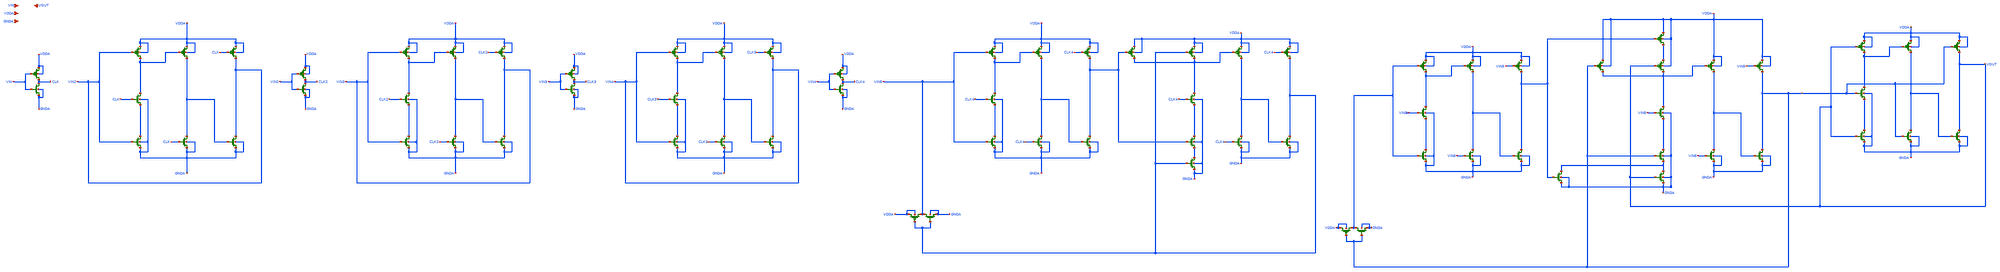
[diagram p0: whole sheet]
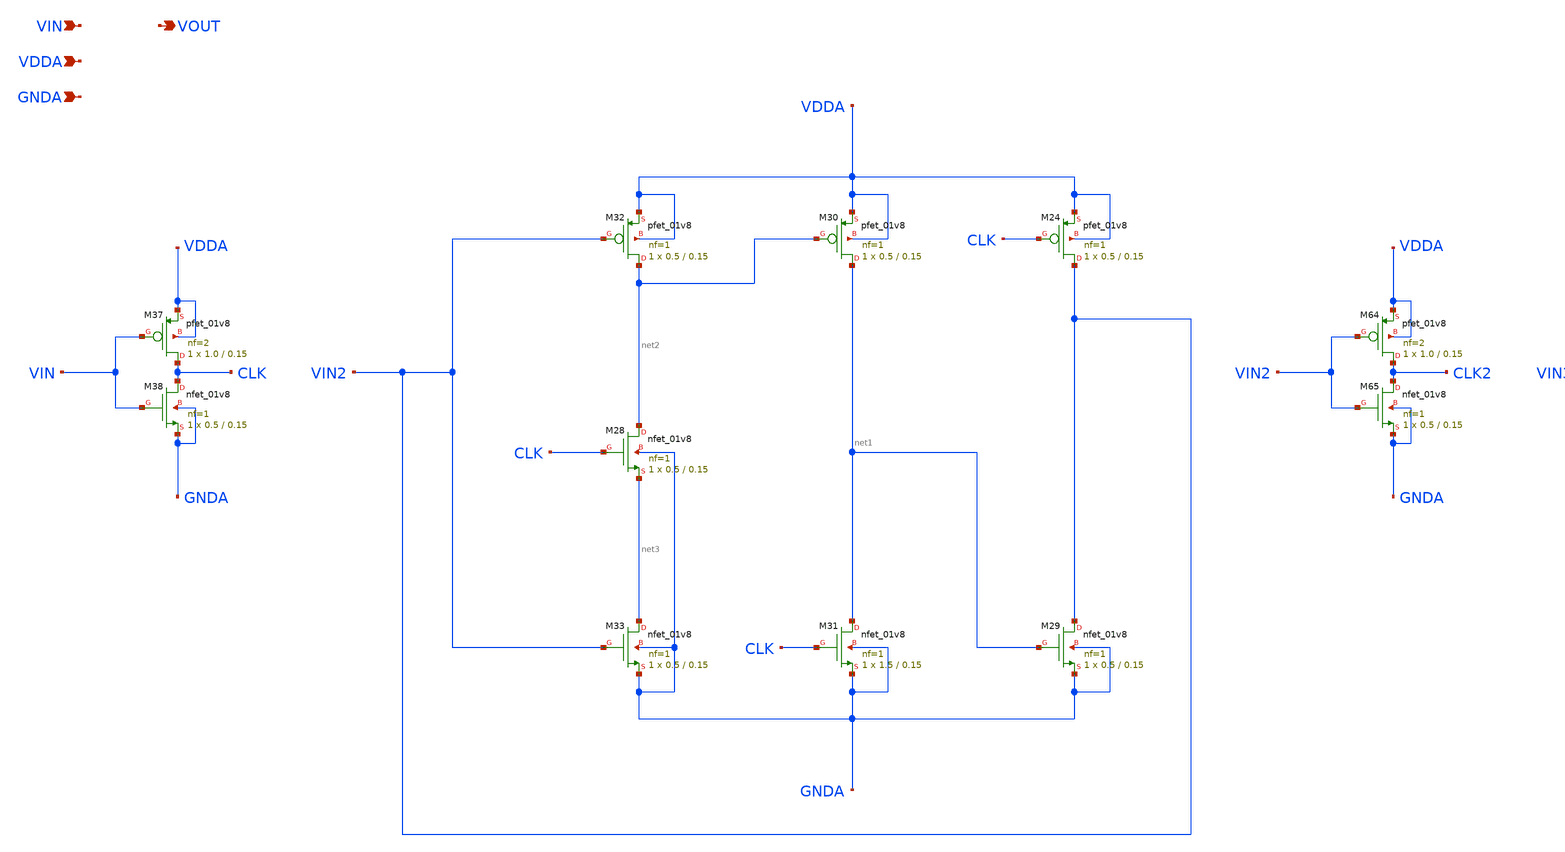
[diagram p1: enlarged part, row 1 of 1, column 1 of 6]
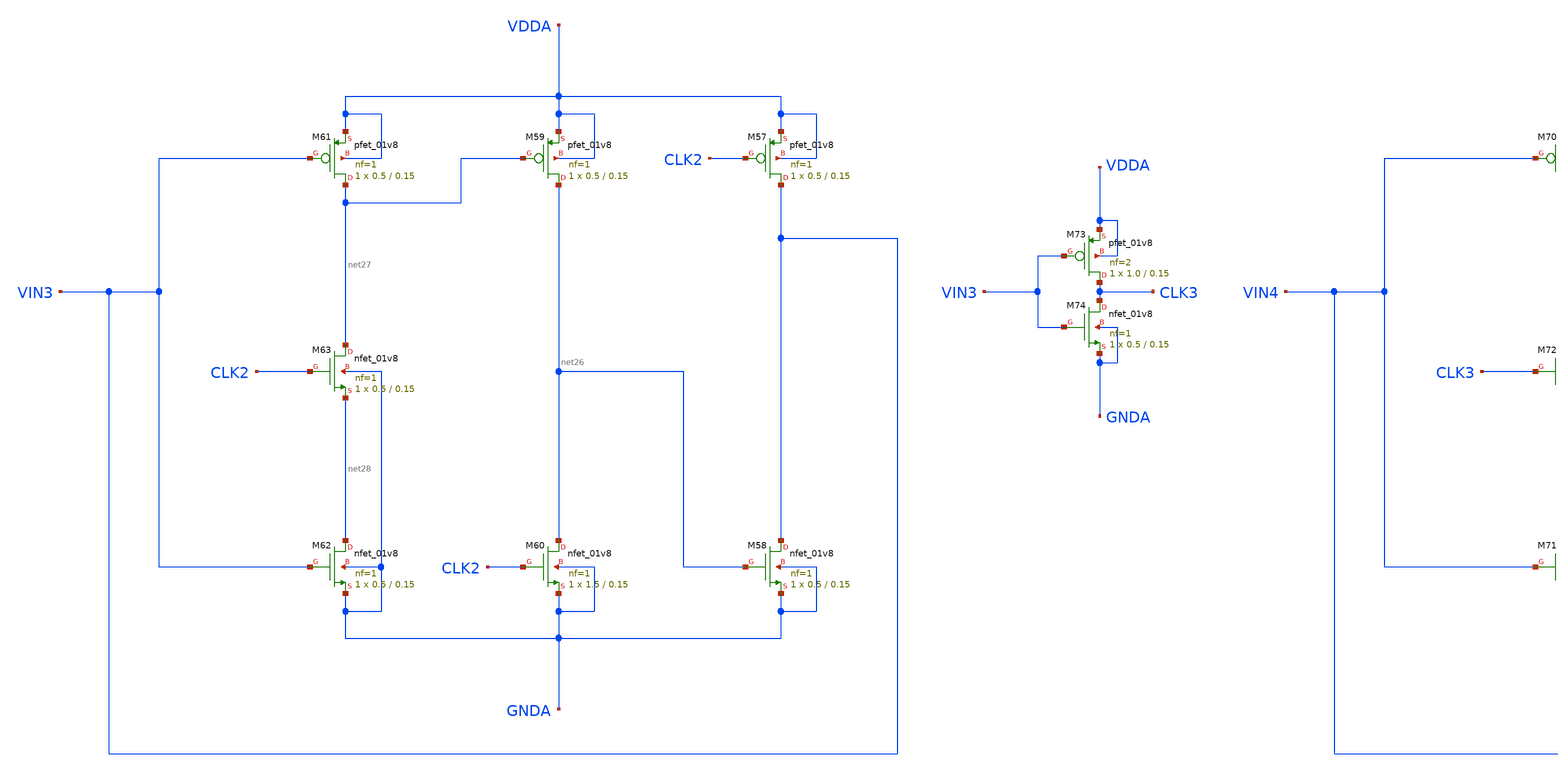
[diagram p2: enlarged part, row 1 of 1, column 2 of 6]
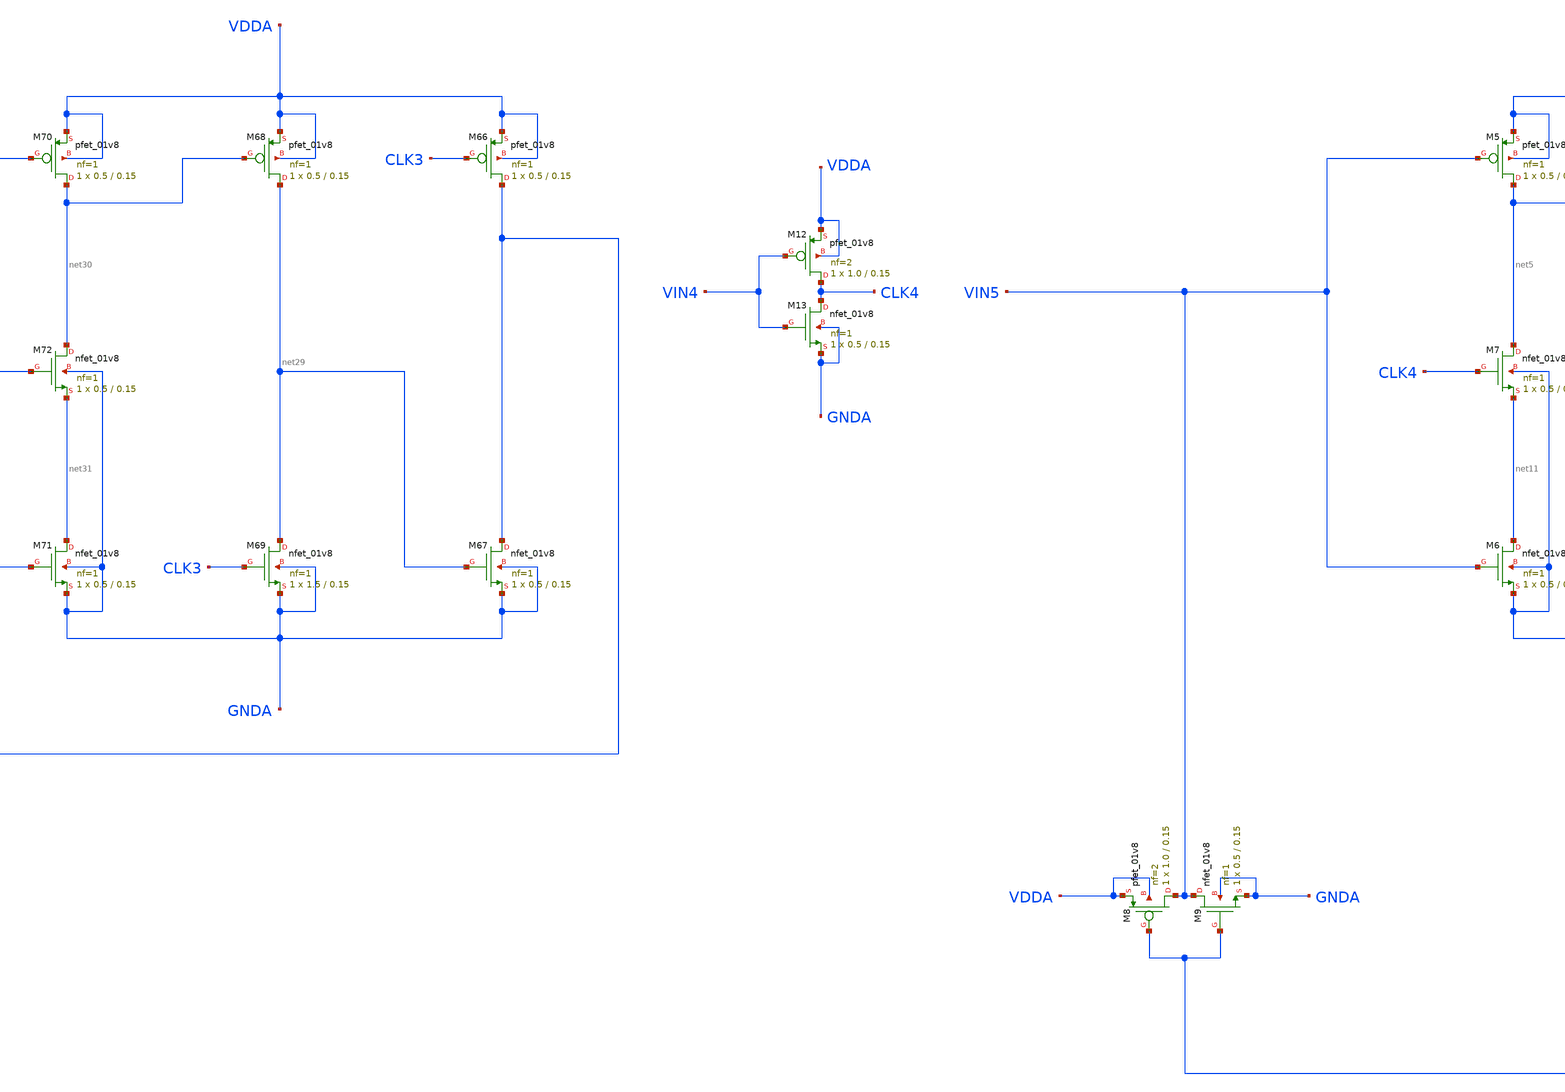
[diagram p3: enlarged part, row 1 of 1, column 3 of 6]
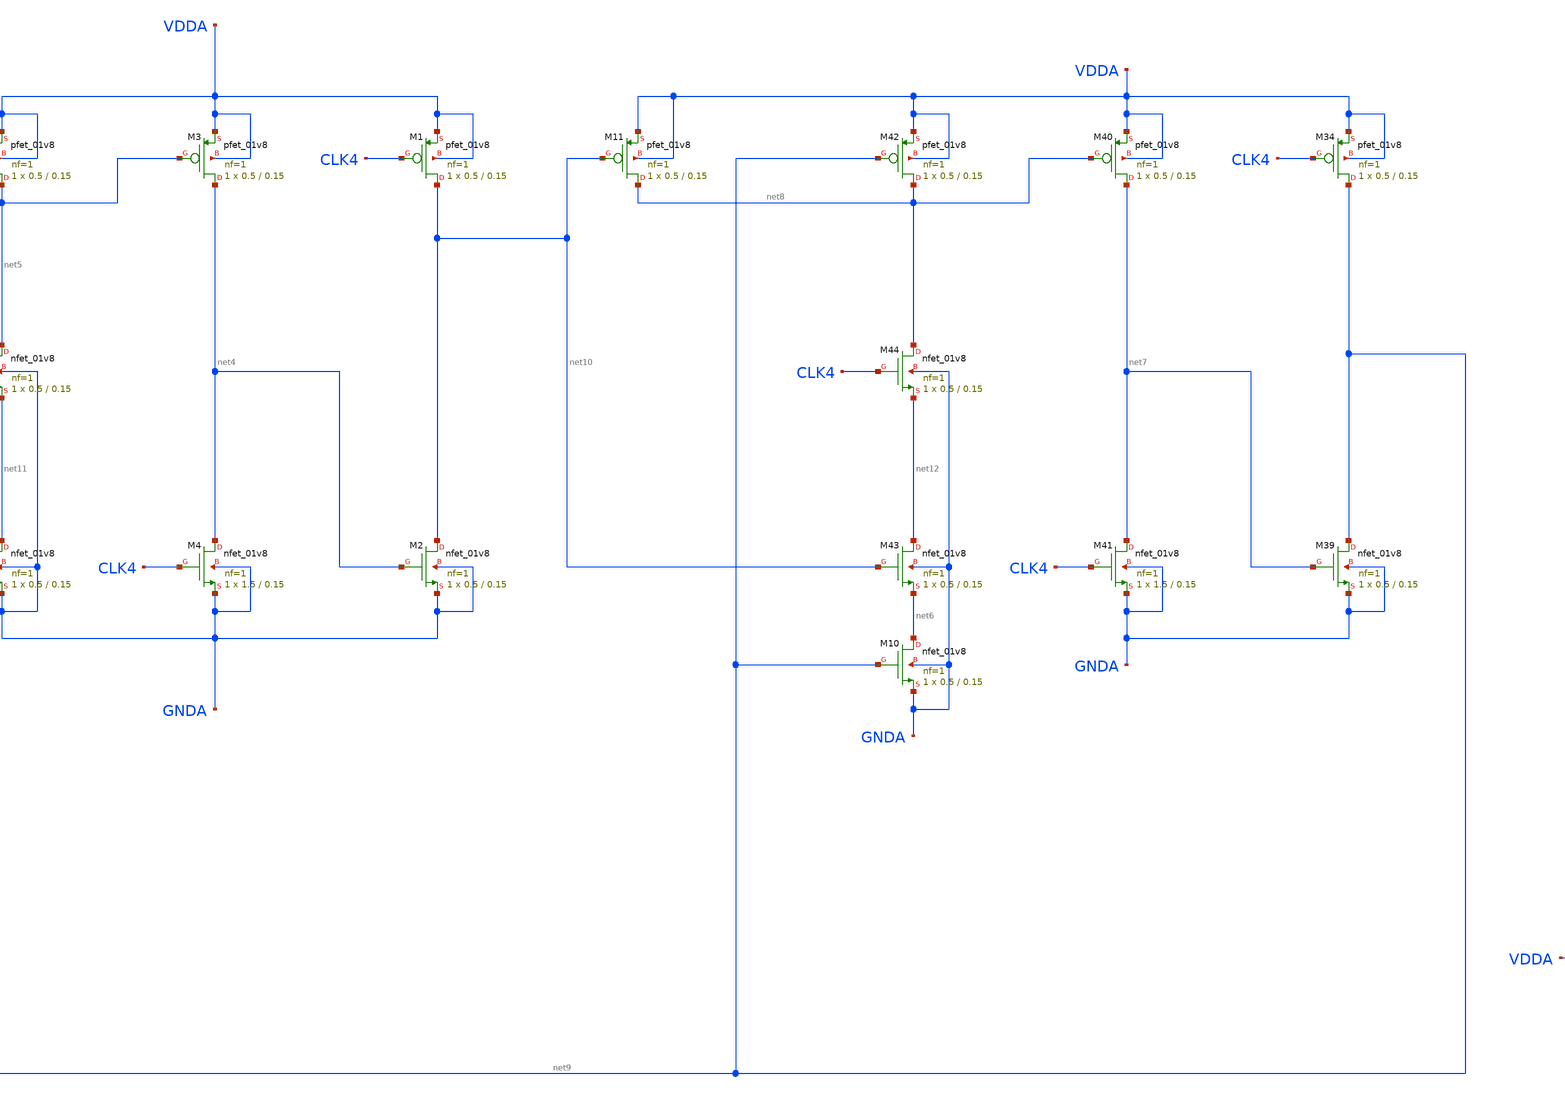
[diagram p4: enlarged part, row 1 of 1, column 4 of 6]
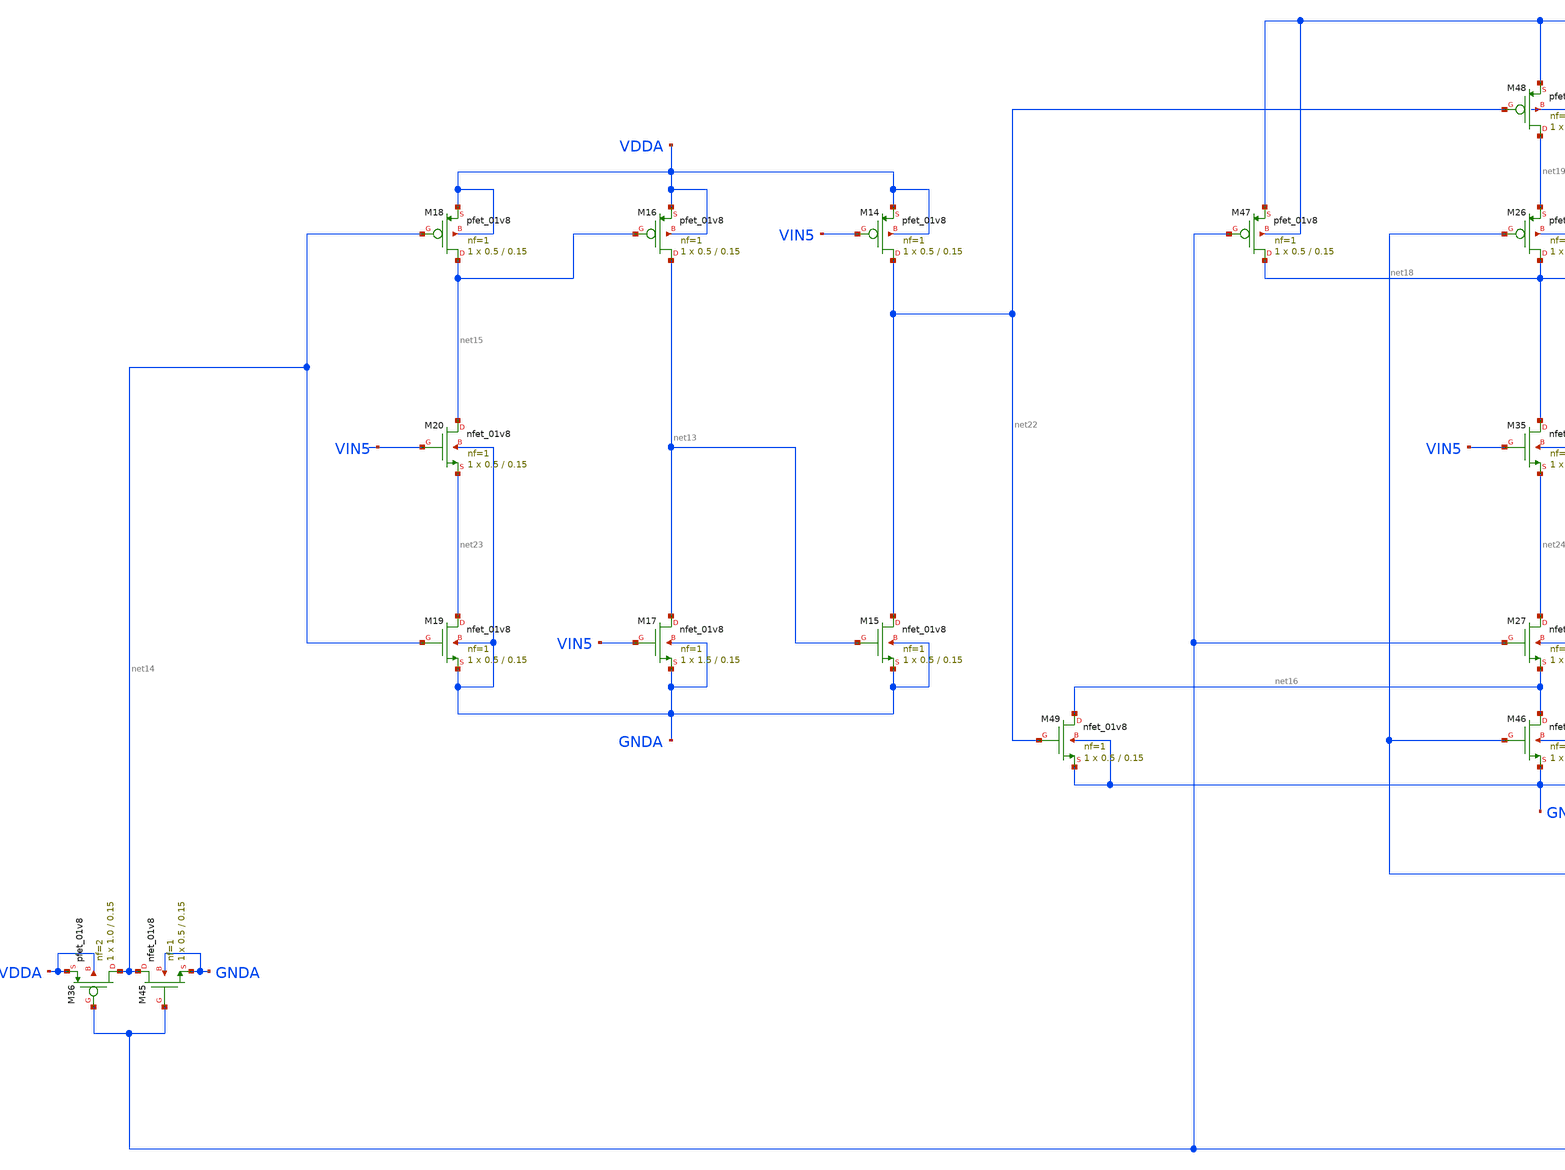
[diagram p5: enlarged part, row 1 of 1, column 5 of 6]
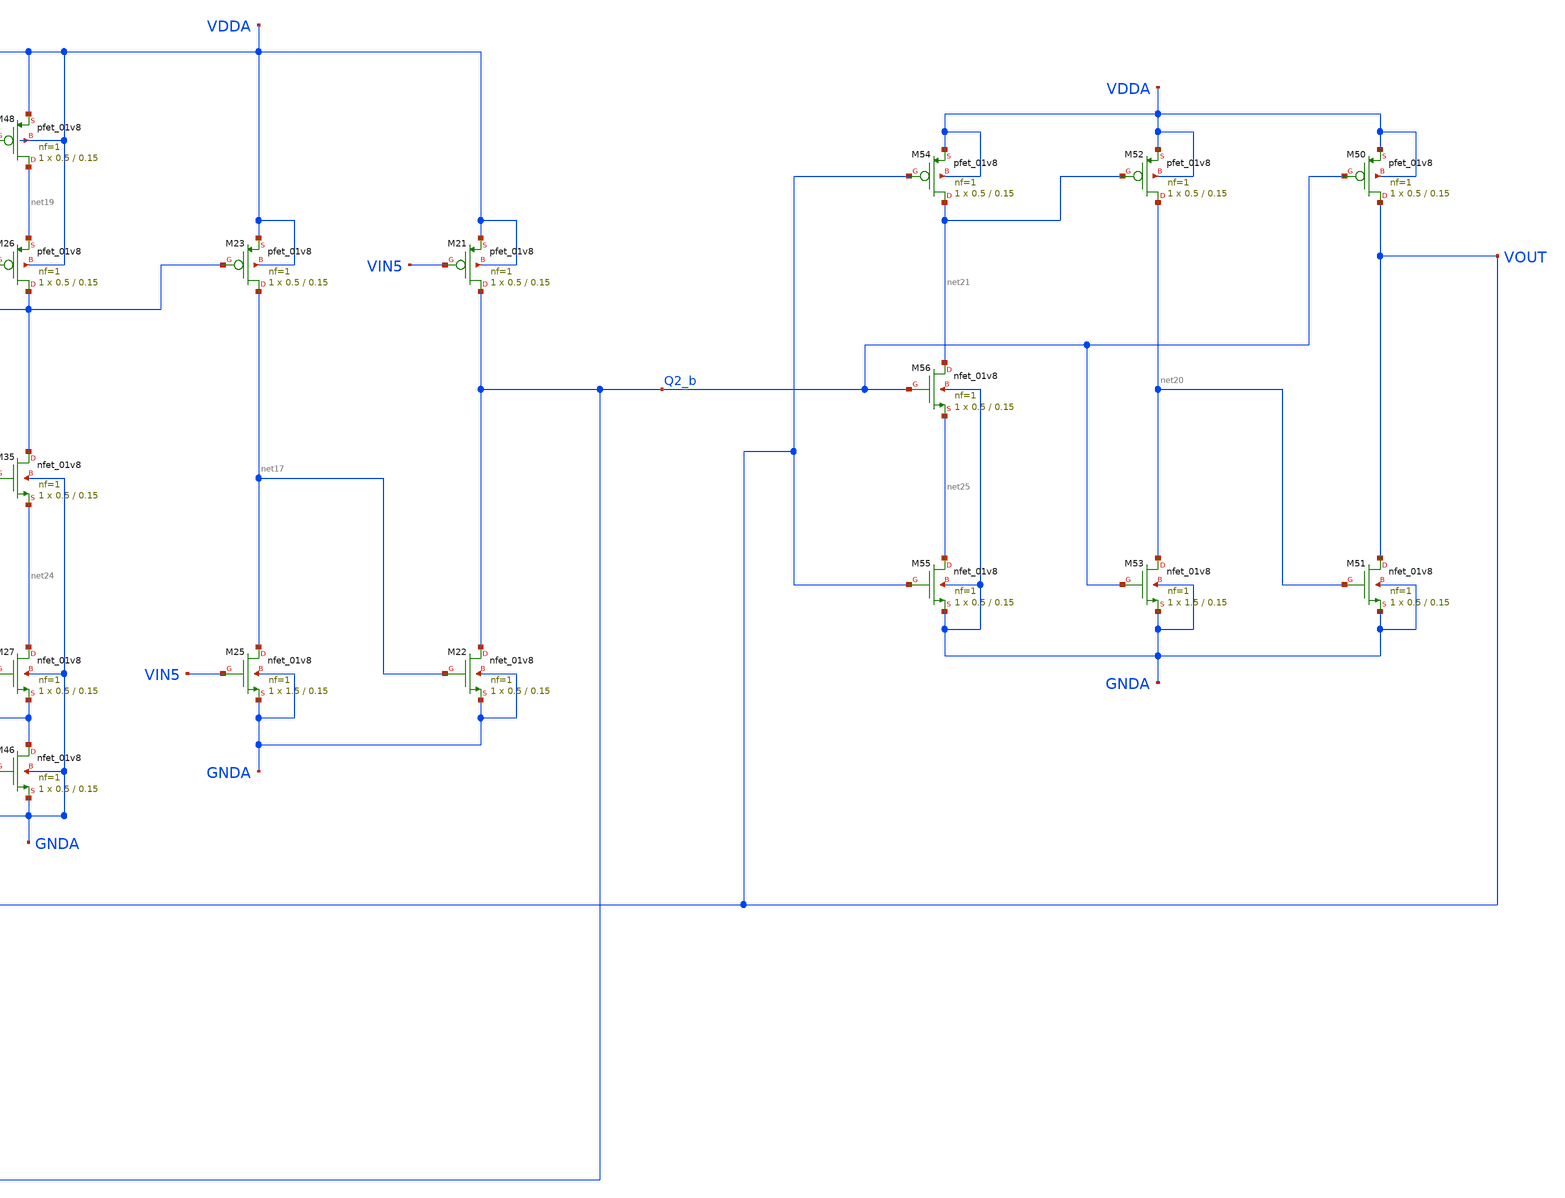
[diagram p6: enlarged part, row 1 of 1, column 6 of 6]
** sch_path: projects/pll/divider/xschem_ngspice/divide_by_120/divide_by_120_xschem.sch
**.subckt divide_by_120_xschem VIN VOUT VDDA GNDA
*.ipin VIN
*.opin VOUT
*.ipin VDDA
*.ipin GNDA
XM24 VIN2 CLK VDDA VDDA sky130_fd_pr__pfet_01v8 L=0.15 W=0.5 nf=1 ad='int((nf+1)/2) * W/nf * 0.29' as='int((nf+2)/2) * W/nf * 0.29'
+ pd='2*int((nf+1)/2) * (W/nf + 0.29)' ps='2*int((nf+2)/2) * (W/nf + 0.29)' nrd='0.29 / W' nrs='0.29 / W'
+ sa=0 sb=0 sd=0 mult=1 m=1
XM29 VIN2 net1 GNDA GNDA sky130_fd_pr__nfet_01v8 L=0.15 W=0.5 nf=1 ad='int((nf+1)/2) * W/nf * 0.29' as='int((nf+2)/2) * W/nf * 0.29'
+ pd='2*int((nf+1)/2) * (W/nf + 0.29)' ps='2*int((nf+2)/2) * (W/nf + 0.29)' nrd='0.29 / W' nrs='0.29 / W'
+ sa=0 sb=0 sd=0 mult=1 m=1
XM30 net1 net2 VDDA VDDA sky130_fd_pr__pfet_01v8 L=0.15 W=0.5 nf=1 ad='int((nf+1)/2) * W/nf * 0.29' as='int((nf+2)/2) * W/nf * 0.29'
+ pd='2*int((nf+1)/2) * (W/nf + 0.29)' ps='2*int((nf+2)/2) * (W/nf + 0.29)' nrd='0.29 / W' nrs='0.29 / W'
+ sa=0 sb=0 sd=0 mult=1 m=1
XM31 net1 CLK GNDA GNDA sky130_fd_pr__nfet_01v8 L=0.15 W=1.5 nf=1 ad='int((nf+1)/2) * W/nf * 0.29' as='int((nf+2)/2) * W/nf * 0.29'
+ pd='2*int((nf+1)/2) * (W/nf + 0.29)' ps='2*int((nf+2)/2) * (W/nf + 0.29)' nrd='0.29 / W' nrs='0.29 / W'
+ sa=0 sb=0 sd=0 mult=1 m=1
XM32 net2 VIN2 VDDA VDDA sky130_fd_pr__pfet_01v8 L=0.15 W=0.5 nf=1 ad='int((nf+1)/2) * W/nf * 0.29' as='int((nf+2)/2) * W/nf * 0.29'
+ pd='2*int((nf+1)/2) * (W/nf + 0.29)' ps='2*int((nf+2)/2) * (W/nf + 0.29)' nrd='0.29 / W' nrs='0.29 / W'
+ sa=0 sb=0 sd=0 mult=1 m=1
XM33 net3 VIN2 GNDA GNDA sky130_fd_pr__nfet_01v8 L=0.15 W=0.5 nf=1 ad='int((nf+1)/2) * W/nf * 0.29' as='int((nf+2)/2) * W/nf * 0.29'
+ pd='2*int((nf+1)/2) * (W/nf + 0.29)' ps='2*int((nf+2)/2) * (W/nf + 0.29)' nrd='0.29 / W' nrs='0.29 / W'
+ sa=0 sb=0 sd=0 mult=1 m=1
XM28 net2 CLK net3 GNDA sky130_fd_pr__nfet_01v8 L=0.15 W=0.5 nf=1 ad='int((nf+1)/2) * W/nf * 0.29' as='int((nf+2)/2) * W/nf * 0.29'
+ pd='2*int((nf+1)/2) * (W/nf + 0.29)' ps='2*int((nf+2)/2) * (W/nf + 0.29)' nrd='0.29 / W' nrs='0.29 / W'
+ sa=0 sb=0 sd=0 mult=1 m=1
XM37 CLK VIN VDDA VDDA sky130_fd_pr__pfet_01v8 L=0.15 W=1.0 nf=2 ad='int((nf+1)/2) * W/nf * 0.29' as='int((nf+2)/2) * W/nf * 0.29'
+ pd='2*int((nf+1)/2) * (W/nf + 0.29)' ps='2*int((nf+2)/2) * (W/nf + 0.29)' nrd='0.29 / W' nrs='0.29 / W'
+ sa=0 sb=0 sd=0 mult=1 m=1
XM38 CLK VIN GNDA GNDA sky130_fd_pr__nfet_01v8 L=0.15 W=0.5 nf=1 ad='int((nf+1)/2) * W/nf * 0.29' as='int((nf+2)/2) * W/nf * 0.29'
+ pd='2*int((nf+1)/2) * (W/nf + 0.29)' ps='2*int((nf+2)/2) * (W/nf + 0.29)' nrd='0.29 / W' nrs='0.29 / W'
+ sa=0 sb=0 sd=0 mult=1 m=1
XM1 net10 CLK4 VDDA VDDA sky130_fd_pr__pfet_01v8 L=0.15 W=0.5 nf=1 ad='int((nf+1)/2) * W/nf * 0.29' as='int((nf+2)/2) * W/nf * 0.29'
+ pd='2*int((nf+1)/2) * (W/nf + 0.29)' ps='2*int((nf+2)/2) * (W/nf + 0.29)' nrd='0.29 / W' nrs='0.29 / W'
+ sa=0 sb=0 sd=0 mult=1 m=1
XM2 net10 net4 GNDA GNDA sky130_fd_pr__nfet_01v8 L=0.15 W=0.5 nf=1 ad='int((nf+1)/2) * W/nf * 0.29' as='int((nf+2)/2) * W/nf * 0.29'
+ pd='2*int((nf+1)/2) * (W/nf + 0.29)' ps='2*int((nf+2)/2) * (W/nf + 0.29)' nrd='0.29 / W' nrs='0.29 / W'
+ sa=0 sb=0 sd=0 mult=1 m=1
XM3 net4 net5 VDDA VDDA sky130_fd_pr__pfet_01v8 L=0.15 W=0.5 nf=1 ad='int((nf+1)/2) * W/nf * 0.29' as='int((nf+2)/2) * W/nf * 0.29'
+ pd='2*int((nf+1)/2) * (W/nf + 0.29)' ps='2*int((nf+2)/2) * (W/nf + 0.29)' nrd='0.29 / W' nrs='0.29 / W'
+ sa=0 sb=0 sd=0 mult=1 m=1
XM4 net4 CLK4 GNDA GNDA sky130_fd_pr__nfet_01v8 L=0.15 W=1.5 nf=1 ad='int((nf+1)/2) * W/nf * 0.29' as='int((nf+2)/2) * W/nf * 0.29'
+ pd='2*int((nf+1)/2) * (W/nf + 0.29)' ps='2*int((nf+2)/2) * (W/nf + 0.29)' nrd='0.29 / W' nrs='0.29 / W'
+ sa=0 sb=0 sd=0 mult=1 m=1
XM5 net5 VIN5 VDDA VDDA sky130_fd_pr__pfet_01v8 L=0.15 W=0.5 nf=1 ad='int((nf+1)/2) * W/nf * 0.29' as='int((nf+2)/2) * W/nf * 0.29'
+ pd='2*int((nf+1)/2) * (W/nf + 0.29)' ps='2*int((nf+2)/2) * (W/nf + 0.29)' nrd='0.29 / W' nrs='0.29 / W'
+ sa=0 sb=0 sd=0 mult=1 m=1
XM6 net11 VIN5 GNDA GNDA sky130_fd_pr__nfet_01v8 L=0.15 W=0.5 nf=1 ad='int((nf+1)/2) * W/nf * 0.29' as='int((nf+2)/2) * W/nf * 0.29'
+ pd='2*int((nf+1)/2) * (W/nf + 0.29)' ps='2*int((nf+2)/2) * (W/nf + 0.29)' nrd='0.29 / W' nrs='0.29 / W'
+ sa=0 sb=0 sd=0 mult=1 m=1
XM7 net5 CLK4 net11 GNDA sky130_fd_pr__nfet_01v8 L=0.15 W=0.5 nf=1 ad='int((nf+1)/2) * W/nf * 0.29' as='int((nf+2)/2) * W/nf * 0.29'
+ pd='2*int((nf+1)/2) * (W/nf + 0.29)' ps='2*int((nf+2)/2) * (W/nf + 0.29)' nrd='0.29 / W' nrs='0.29 / W'
+ sa=0 sb=0 sd=0 mult=1 m=1
XM34 net9 CLK4 VDDA VDDA sky130_fd_pr__pfet_01v8 L=0.15 W=0.5 nf=1 ad='int((nf+1)/2) * W/nf * 0.29' as='int((nf+2)/2) * W/nf * 0.29'
+ pd='2*int((nf+1)/2) * (W/nf + 0.29)' ps='2*int((nf+2)/2) * (W/nf + 0.29)' nrd='0.29 / W' nrs='0.29 / W'
+ sa=0 sb=0 sd=0 mult=1 m=1
XM39 net9 net7 GNDA GNDA sky130_fd_pr__nfet_01v8 L=0.15 W=0.5 nf=1 ad='int((nf+1)/2) * W/nf * 0.29' as='int((nf+2)/2) * W/nf * 0.29'
+ pd='2*int((nf+1)/2) * (W/nf + 0.29)' ps='2*int((nf+2)/2) * (W/nf + 0.29)' nrd='0.29 / W' nrs='0.29 / W'
+ sa=0 sb=0 sd=0 mult=1 m=1
XM40 net7 net8 VDDA VDDA sky130_fd_pr__pfet_01v8 L=0.15 W=0.5 nf=1 ad='int((nf+1)/2) * W/nf * 0.29' as='int((nf+2)/2) * W/nf * 0.29'
+ pd='2*int((nf+1)/2) * (W/nf + 0.29)' ps='2*int((nf+2)/2) * (W/nf + 0.29)' nrd='0.29 / W' nrs='0.29 / W'
+ sa=0 sb=0 sd=0 mult=1 m=1
XM41 net7 CLK4 GNDA GNDA sky130_fd_pr__nfet_01v8 L=0.15 W=1.5 nf=1 ad='int((nf+1)/2) * W/nf * 0.29' as='int((nf+2)/2) * W/nf * 0.29'
+ pd='2*int((nf+1)/2) * (W/nf + 0.29)' ps='2*int((nf+2)/2) * (W/nf + 0.29)' nrd='0.29 / W' nrs='0.29 / W'
+ sa=0 sb=0 sd=0 mult=1 m=1
XM42 net8 net9 VDDA VDDA sky130_fd_pr__pfet_01v8 L=0.15 W=0.5 nf=1 ad='int((nf+1)/2) * W/nf * 0.29' as='int((nf+2)/2) * W/nf * 0.29'
+ pd='2*int((nf+1)/2) * (W/nf + 0.29)' ps='2*int((nf+2)/2) * (W/nf + 0.29)' nrd='0.29 / W' nrs='0.29 / W'
+ sa=0 sb=0 sd=0 mult=1 m=1
XM43 net12 net10 net6 GNDA sky130_fd_pr__nfet_01v8 L=0.15 W=0.5 nf=1 ad='int((nf+1)/2) * W/nf * 0.29'
+ as='int((nf+2)/2) * W/nf * 0.29' pd='2*int((nf+1)/2) * (W/nf + 0.29)' ps='2*int((nf+2)/2) * (W/nf + 0.29)'
+ nrd='0.29 / W' nrs='0.29 / W' sa=0 sb=0 sd=0 mult=1 m=1
XM44 net8 CLK4 net12 GNDA sky130_fd_pr__nfet_01v8 L=0.15 W=0.5 nf=1 ad='int((nf+1)/2) * W/nf * 0.29'
+ as='int((nf+2)/2) * W/nf * 0.29' pd='2*int((nf+1)/2) * (W/nf + 0.29)' ps='2*int((nf+2)/2) * (W/nf + 0.29)'
+ nrd='0.29 / W' nrs='0.29 / W' sa=0 sb=0 sd=0 mult=1 m=1
XM8 VIN5 net9 VDDA VDDA sky130_fd_pr__pfet_01v8 L=0.15 W=1.0 nf=2 ad='int((nf+1)/2) * W/nf * 0.29' as='int((nf+2)/2) * W/nf * 0.29'
+ pd='2*int((nf+1)/2) * (W/nf + 0.29)' ps='2*int((nf+2)/2) * (W/nf + 0.29)' nrd='0.29 / W' nrs='0.29 / W'
+ sa=0 sb=0 sd=0 mult=1 m=1
XM9 VIN5 net9 GNDA GNDA sky130_fd_pr__nfet_01v8 L=0.15 W=0.5 nf=1 ad='int((nf+1)/2) * W/nf * 0.29' as='int((nf+2)/2) * W/nf * 0.29'
+ pd='2*int((nf+1)/2) * (W/nf + 0.29)' ps='2*int((nf+2)/2) * (W/nf + 0.29)' nrd='0.29 / W' nrs='0.29 / W'
+ sa=0 sb=0 sd=0 mult=1 m=1
XM10 net6 net9 GNDA GNDA sky130_fd_pr__nfet_01v8 L=0.15 W=0.5 nf=1 ad='int((nf+1)/2) * W/nf * 0.29' as='int((nf+2)/2) * W/nf * 0.29'
+ pd='2*int((nf+1)/2) * (W/nf + 0.29)' ps='2*int((nf+2)/2) * (W/nf + 0.29)' nrd='0.29 / W' nrs='0.29 / W'
+ sa=0 sb=0 sd=0 mult=1 m=1
XM11 net8 net10 VDDA VDDA sky130_fd_pr__pfet_01v8 L=0.15 W=0.5 nf=1 ad='int((nf+1)/2) * W/nf * 0.29'
+ as='int((nf+2)/2) * W/nf * 0.29' pd='2*int((nf+1)/2) * (W/nf + 0.29)' ps='2*int((nf+2)/2) * (W/nf + 0.29)'
+ nrd='0.29 / W' nrs='0.29 / W' sa=0 sb=0 sd=0 mult=1 m=1
XM12 CLK4 VIN4 VDDA VDDA sky130_fd_pr__pfet_01v8 L=0.15 W=1.0 nf=2 ad='int((nf+1)/2) * W/nf * 0.29' as='int((nf+2)/2) * W/nf * 0.29'
+ pd='2*int((nf+1)/2) * (W/nf + 0.29)' ps='2*int((nf+2)/2) * (W/nf + 0.29)' nrd='0.29 / W' nrs='0.29 / W'
+ sa=0 sb=0 sd=0 mult=1 m=1
XM13 CLK4 VIN4 GNDA GNDA sky130_fd_pr__nfet_01v8 L=0.15 W=0.5 nf=1 ad='int((nf+1)/2) * W/nf * 0.29' as='int((nf+2)/2) * W/nf * 0.29'
+ pd='2*int((nf+1)/2) * (W/nf + 0.29)' ps='2*int((nf+2)/2) * (W/nf + 0.29)' nrd='0.29 / W' nrs='0.29 / W'
+ sa=0 sb=0 sd=0 mult=1 m=1
XM14 net22 VIN5 VDDA VDDA sky130_fd_pr__pfet_01v8 L=0.15 W=0.5 nf=1 ad='int((nf+1)/2) * W/nf * 0.29'
+ as='int((nf+2)/2) * W/nf * 0.29' pd='2*int((nf+1)/2) * (W/nf + 0.29)' ps='2*int((nf+2)/2) * (W/nf + 0.29)'
+ nrd='0.29 / W' nrs='0.29 / W' sa=0 sb=0 sd=0 mult=1 m=1
XM15 net22 net13 GNDA GNDA sky130_fd_pr__nfet_01v8 L=0.15 W=0.5 nf=1 ad='int((nf+1)/2) * W/nf * 0.29'
+ as='int((nf+2)/2) * W/nf * 0.29' pd='2*int((nf+1)/2) * (W/nf + 0.29)' ps='2*int((nf+2)/2) * (W/nf + 0.29)'
+ nrd='0.29 / W' nrs='0.29 / W' sa=0 sb=0 sd=0 mult=1 m=1
XM16 net13 net15 VDDA VDDA sky130_fd_pr__pfet_01v8 L=0.15 W=0.5 nf=1 ad='int((nf+1)/2) * W/nf * 0.29'
+ as='int((nf+2)/2) * W/nf * 0.29' pd='2*int((nf+1)/2) * (W/nf + 0.29)' ps='2*int((nf+2)/2) * (W/nf + 0.29)'
+ nrd='0.29 / W' nrs='0.29 / W' sa=0 sb=0 sd=0 mult=1 m=1
XM17 net13 VIN5 GNDA GNDA sky130_fd_pr__nfet_01v8 L=0.15 W=1.5 nf=1 ad='int((nf+1)/2) * W/nf * 0.29'
+ as='int((nf+2)/2) * W/nf * 0.29' pd='2*int((nf+1)/2) * (W/nf + 0.29)' ps='2*int((nf+2)/2) * (W/nf + 0.29)'
+ nrd='0.29 / W' nrs='0.29 / W' sa=0 sb=0 sd=0 mult=1 m=1
XM18 net15 net14 VDDA VDDA sky130_fd_pr__pfet_01v8 L=0.15 W=0.5 nf=1 ad='int((nf+1)/2) * W/nf * 0.29'
+ as='int((nf+2)/2) * W/nf * 0.29' pd='2*int((nf+1)/2) * (W/nf + 0.29)' ps='2*int((nf+2)/2) * (W/nf + 0.29)'
+ nrd='0.29 / W' nrs='0.29 / W' sa=0 sb=0 sd=0 mult=1 m=1
XM19 net23 net14 GNDA GNDA sky130_fd_pr__nfet_01v8 L=0.15 W=0.5 nf=1 ad='int((nf+1)/2) * W/nf * 0.29'
+ as='int((nf+2)/2) * W/nf * 0.29' pd='2*int((nf+1)/2) * (W/nf + 0.29)' ps='2*int((nf+2)/2) * (W/nf + 0.29)'
+ nrd='0.29 / W' nrs='0.29 / W' sa=0 sb=0 sd=0 mult=1 m=1
XM20 net15 VIN5 net23 GNDA sky130_fd_pr__nfet_01v8 L=0.15 W=0.5 nf=1 ad='int((nf+1)/2) * W/nf * 0.29'
+ as='int((nf+2)/2) * W/nf * 0.29' pd='2*int((nf+1)/2) * (W/nf + 0.29)' ps='2*int((nf+2)/2) * (W/nf + 0.29)'
+ nrd='0.29 / W' nrs='0.29 / W' sa=0 sb=0 sd=0 mult=1 m=1
XM21 Q2_b VIN5 VDDA VDDA sky130_fd_pr__pfet_01v8 L=0.15 W=0.5 nf=1 ad='int((nf+1)/2) * W/nf * 0.29' as='int((nf+2)/2) * W/nf * 0.29'
+ pd='2*int((nf+1)/2) * (W/nf + 0.29)' ps='2*int((nf+2)/2) * (W/nf + 0.29)' nrd='0.29 / W' nrs='0.29 / W'
+ sa=0 sb=0 sd=0 mult=1 m=1
XM22 Q2_b net17 GNDA GNDA sky130_fd_pr__nfet_01v8 L=0.15 W=0.5 nf=1 ad='int((nf+1)/2) * W/nf * 0.29'
+ as='int((nf+2)/2) * W/nf * 0.29' pd='2*int((nf+1)/2) * (W/nf + 0.29)' ps='2*int((nf+2)/2) * (W/nf + 0.29)'
+ nrd='0.29 / W' nrs='0.29 / W' sa=0 sb=0 sd=0 mult=1 m=1
XM23 net17 net18 VDDA VDDA sky130_fd_pr__pfet_01v8 L=0.15 W=0.5 nf=1 ad='int((nf+1)/2) * W/nf * 0.29'
+ as='int((nf+2)/2) * W/nf * 0.29' pd='2*int((nf+1)/2) * (W/nf + 0.29)' ps='2*int((nf+2)/2) * (W/nf + 0.29)'
+ nrd='0.29 / W' nrs='0.29 / W' sa=0 sb=0 sd=0 mult=1 m=1
XM25 net17 VIN5 GNDA GNDA sky130_fd_pr__nfet_01v8 L=0.15 W=1.5 nf=1 ad='int((nf+1)/2) * W/nf * 0.29'
+ as='int((nf+2)/2) * W/nf * 0.29' pd='2*int((nf+1)/2) * (W/nf + 0.29)' ps='2*int((nf+2)/2) * (W/nf + 0.29)'
+ nrd='0.29 / W' nrs='0.29 / W' sa=0 sb=0 sd=0 mult=1 m=1
XM26 net18 VOUT net19 VDDA sky130_fd_pr__pfet_01v8 L=0.15 W=0.5 nf=1 ad='int((nf+1)/2) * W/nf * 0.29'
+ as='int((nf+2)/2) * W/nf * 0.29' pd='2*int((nf+1)/2) * (W/nf + 0.29)' ps='2*int((nf+2)/2) * (W/nf + 0.29)'
+ nrd='0.29 / W' nrs='0.29 / W' sa=0 sb=0 sd=0 mult=1 m=1
XM27 net24 Q2_b net16 GNDA sky130_fd_pr__nfet_01v8 L=0.15 W=0.5 nf=1 ad='int((nf+1)/2) * W/nf * 0.29'
+ as='int((nf+2)/2) * W/nf * 0.29' pd='2*int((nf+1)/2) * (W/nf + 0.29)' ps='2*int((nf+2)/2) * (W/nf + 0.29)'
+ nrd='0.29 / W' nrs='0.29 / W' sa=0 sb=0 sd=0 mult=1 m=1
XM35 net18 VIN5 net24 GNDA sky130_fd_pr__nfet_01v8 L=0.15 W=0.5 nf=1 ad='int((nf+1)/2) * W/nf * 0.29'
+ as='int((nf+2)/2) * W/nf * 0.29' pd='2*int((nf+1)/2) * (W/nf + 0.29)' ps='2*int((nf+2)/2) * (W/nf + 0.29)'
+ nrd='0.29 / W' nrs='0.29 / W' sa=0 sb=0 sd=0 mult=1 m=1
XM36 net14 Q2_b VDDA VDDA sky130_fd_pr__pfet_01v8 L=0.15 W=1.0 nf=2 ad='int((nf+1)/2) * W/nf * 0.29'
+ as='int((nf+2)/2) * W/nf * 0.29' pd='2*int((nf+1)/2) * (W/nf + 0.29)' ps='2*int((nf+2)/2) * (W/nf + 0.29)'
+ nrd='0.29 / W' nrs='0.29 / W' sa=0 sb=0 sd=0 mult=1 m=1
XM45 net14 Q2_b GNDA GNDA sky130_fd_pr__nfet_01v8 L=0.15 W=0.5 nf=1 ad='int((nf+1)/2) * W/nf * 0.29'
+ as='int((nf+2)/2) * W/nf * 0.29' pd='2*int((nf+1)/2) * (W/nf + 0.29)' ps='2*int((nf+2)/2) * (W/nf + 0.29)'
+ nrd='0.29 / W' nrs='0.29 / W' sa=0 sb=0 sd=0 mult=1 m=1
XM46 net16 VOUT GNDA GNDA sky130_fd_pr__nfet_01v8 L=0.15 W=0.5 nf=1 ad='int((nf+1)/2) * W/nf * 0.29'
+ as='int((nf+2)/2) * W/nf * 0.29' pd='2*int((nf+1)/2) * (W/nf + 0.29)' ps='2*int((nf+2)/2) * (W/nf + 0.29)'
+ nrd='0.29 / W' nrs='0.29 / W' sa=0 sb=0 sd=0 mult=1 m=1
XM47 net18 Q2_b VDDA VDDA sky130_fd_pr__pfet_01v8 L=0.15 W=0.5 nf=1 ad='int((nf+1)/2) * W/nf * 0.29'
+ as='int((nf+2)/2) * W/nf * 0.29' pd='2*int((nf+1)/2) * (W/nf + 0.29)' ps='2*int((nf+2)/2) * (W/nf + 0.29)'
+ nrd='0.29 / W' nrs='0.29 / W' sa=0 sb=0 sd=0 mult=1 m=1
XM48 net19 net22 VDDA VDDA sky130_fd_pr__pfet_01v8 L=0.15 W=0.5 nf=1 ad='int((nf+1)/2) * W/nf * 0.29'
+ as='int((nf+2)/2) * W/nf * 0.29' pd='2*int((nf+1)/2) * (W/nf + 0.29)' ps='2*int((nf+2)/2) * (W/nf + 0.29)'
+ nrd='0.29 / W' nrs='0.29 / W' sa=0 sb=0 sd=0 mult=1 m=1
XM49 net16 net22 GNDA GNDA sky130_fd_pr__nfet_01v8 L=0.15 W=0.5 nf=1 ad='int((nf+1)/2) * W/nf * 0.29'
+ as='int((nf+2)/2) * W/nf * 0.29' pd='2*int((nf+1)/2) * (W/nf + 0.29)' ps='2*int((nf+2)/2) * (W/nf + 0.29)'
+ nrd='0.29 / W' nrs='0.29 / W' sa=0 sb=0 sd=0 mult=1 m=1
XM50 VOUT Q2_b VDDA VDDA sky130_fd_pr__pfet_01v8 L=0.15 W=0.5 nf=1 ad='int((nf+1)/2) * W/nf * 0.29' as='int((nf+2)/2) * W/nf * 0.29'
+ pd='2*int((nf+1)/2) * (W/nf + 0.29)' ps='2*int((nf+2)/2) * (W/nf + 0.29)' nrd='0.29 / W' nrs='0.29 / W'
+ sa=0 sb=0 sd=0 mult=1 m=1
XM51 VOUT net20 GNDA GNDA sky130_fd_pr__nfet_01v8 L=0.15 W=0.5 nf=1 ad='int((nf+1)/2) * W/nf * 0.29'
+ as='int((nf+2)/2) * W/nf * 0.29' pd='2*int((nf+1)/2) * (W/nf + 0.29)' ps='2*int((nf+2)/2) * (W/nf + 0.29)'
+ nrd='0.29 / W' nrs='0.29 / W' sa=0 sb=0 sd=0 mult=1 m=1
XM52 net20 net21 VDDA VDDA sky130_fd_pr__pfet_01v8 L=0.15 W=0.5 nf=1 ad='int((nf+1)/2) * W/nf * 0.29'
+ as='int((nf+2)/2) * W/nf * 0.29' pd='2*int((nf+1)/2) * (W/nf + 0.29)' ps='2*int((nf+2)/2) * (W/nf + 0.29)'
+ nrd='0.29 / W' nrs='0.29 / W' sa=0 sb=0 sd=0 mult=1 m=1
XM53 net20 Q2_b GNDA GNDA sky130_fd_pr__nfet_01v8 L=0.15 W=1.5 nf=1 ad='int((nf+1)/2) * W/nf * 0.29'
+ as='int((nf+2)/2) * W/nf * 0.29' pd='2*int((nf+1)/2) * (W/nf + 0.29)' ps='2*int((nf+2)/2) * (W/nf + 0.29)'
+ nrd='0.29 / W' nrs='0.29 / W' sa=0 sb=0 sd=0 mult=1 m=1
XM54 net21 VOUT VDDA VDDA sky130_fd_pr__pfet_01v8 L=0.15 W=0.5 nf=1 ad='int((nf+1)/2) * W/nf * 0.29'
+ as='int((nf+2)/2) * W/nf * 0.29' pd='2*int((nf+1)/2) * (W/nf + 0.29)' ps='2*int((nf+2)/2) * (W/nf + 0.29)'
+ nrd='0.29 / W' nrs='0.29 / W' sa=0 sb=0 sd=0 mult=1 m=1
XM55 net25 VOUT GNDA GNDA sky130_fd_pr__nfet_01v8 L=0.15 W=0.5 nf=1 ad='int((nf+1)/2) * W/nf * 0.29'
+ as='int((nf+2)/2) * W/nf * 0.29' pd='2*int((nf+1)/2) * (W/nf + 0.29)' ps='2*int((nf+2)/2) * (W/nf + 0.29)'
+ nrd='0.29 / W' nrs='0.29 / W' sa=0 sb=0 sd=0 mult=1 m=1
XM56 net21 Q2_b net25 GNDA sky130_fd_pr__nfet_01v8 L=0.15 W=0.5 nf=1 ad='int((nf+1)/2) * W/nf * 0.29'
+ as='int((nf+2)/2) * W/nf * 0.29' pd='2*int((nf+1)/2) * (W/nf + 0.29)' ps='2*int((nf+2)/2) * (W/nf + 0.29)'
+ nrd='0.29 / W' nrs='0.29 / W' sa=0 sb=0 sd=0 mult=1 m=1
XM57 VIN3 CLK2 VDDA VDDA sky130_fd_pr__pfet_01v8 L=0.15 W=0.5 nf=1 ad='int((nf+1)/2) * W/nf * 0.29' as='int((nf+2)/2) * W/nf * 0.29'
+ pd='2*int((nf+1)/2) * (W/nf + 0.29)' ps='2*int((nf+2)/2) * (W/nf + 0.29)' nrd='0.29 / W' nrs='0.29 / W'
+ sa=0 sb=0 sd=0 mult=1 m=1
XM58 VIN3 net26 GNDA GNDA sky130_fd_pr__nfet_01v8 L=0.15 W=0.5 nf=1 ad='int((nf+1)/2) * W/nf * 0.29'
+ as='int((nf+2)/2) * W/nf * 0.29' pd='2*int((nf+1)/2) * (W/nf + 0.29)' ps='2*int((nf+2)/2) * (W/nf + 0.29)'
+ nrd='0.29 / W' nrs='0.29 / W' sa=0 sb=0 sd=0 mult=1 m=1
XM59 net26 net27 VDDA VDDA sky130_fd_pr__pfet_01v8 L=0.15 W=0.5 nf=1 ad='int((nf+1)/2) * W/nf * 0.29'
+ as='int((nf+2)/2) * W/nf * 0.29' pd='2*int((nf+1)/2) * (W/nf + 0.29)' ps='2*int((nf+2)/2) * (W/nf + 0.29)'
+ nrd='0.29 / W' nrs='0.29 / W' sa=0 sb=0 sd=0 mult=1 m=1
XM60 net26 CLK2 GNDA GNDA sky130_fd_pr__nfet_01v8 L=0.15 W=1.5 nf=1 ad='int((nf+1)/2) * W/nf * 0.29'
+ as='int((nf+2)/2) * W/nf * 0.29' pd='2*int((nf+1)/2) * (W/nf + 0.29)' ps='2*int((nf+2)/2) * (W/nf + 0.29)'
+ nrd='0.29 / W' nrs='0.29 / W' sa=0 sb=0 sd=0 mult=1 m=1
XM61 net27 VIN3 VDDA VDDA sky130_fd_pr__pfet_01v8 L=0.15 W=0.5 nf=1 ad='int((nf+1)/2) * W/nf * 0.29'
+ as='int((nf+2)/2) * W/nf * 0.29' pd='2*int((nf+1)/2) * (W/nf + 0.29)' ps='2*int((nf+2)/2) * (W/nf + 0.29)'
+ nrd='0.29 / W' nrs='0.29 / W' sa=0 sb=0 sd=0 mult=1 m=1
XM62 net28 VIN3 GNDA GNDA sky130_fd_pr__nfet_01v8 L=0.15 W=0.5 nf=1 ad='int((nf+1)/2) * W/nf * 0.29'
+ as='int((nf+2)/2) * W/nf * 0.29' pd='2*int((nf+1)/2) * (W/nf + 0.29)' ps='2*int((nf+2)/2) * (W/nf + 0.29)'
+ nrd='0.29 / W' nrs='0.29 / W' sa=0 sb=0 sd=0 mult=1 m=1
XM63 net27 CLK2 net28 GNDA sky130_fd_pr__nfet_01v8 L=0.15 W=0.5 nf=1 ad='int((nf+1)/2) * W/nf * 0.29'
+ as='int((nf+2)/2) * W/nf * 0.29' pd='2*int((nf+1)/2) * (W/nf + 0.29)' ps='2*int((nf+2)/2) * (W/nf + 0.29)'
+ nrd='0.29 / W' nrs='0.29 / W' sa=0 sb=0 sd=0 mult=1 m=1
XM64 CLK2 VIN2 VDDA VDDA sky130_fd_pr__pfet_01v8 L=0.15 W=1.0 nf=2 ad='int((nf+1)/2) * W/nf * 0.29' as='int((nf+2)/2) * W/nf * 0.29'
+ pd='2*int((nf+1)/2) * (W/nf + 0.29)' ps='2*int((nf+2)/2) * (W/nf + 0.29)' nrd='0.29 / W' nrs='0.29 / W'
+ sa=0 sb=0 sd=0 mult=1 m=1
XM65 CLK2 VIN2 GNDA GNDA sky130_fd_pr__nfet_01v8 L=0.15 W=0.5 nf=1 ad='int((nf+1)/2) * W/nf * 0.29' as='int((nf+2)/2) * W/nf * 0.29'
+ pd='2*int((nf+1)/2) * (W/nf + 0.29)' ps='2*int((nf+2)/2) * (W/nf + 0.29)' nrd='0.29 / W' nrs='0.29 / W'
+ sa=0 sb=0 sd=0 mult=1 m=1
XM66 VIN4 CLK3 VDDA VDDA sky130_fd_pr__pfet_01v8 L=0.15 W=0.5 nf=1 ad='int((nf+1)/2) * W/nf * 0.29' as='int((nf+2)/2) * W/nf * 0.29'
+ pd='2*int((nf+1)/2) * (W/nf + 0.29)' ps='2*int((nf+2)/2) * (W/nf + 0.29)' nrd='0.29 / W' nrs='0.29 / W'
+ sa=0 sb=0 sd=0 mult=1 m=1
XM67 VIN4 net29 GNDA GNDA sky130_fd_pr__nfet_01v8 L=0.15 W=0.5 nf=1 ad='int((nf+1)/2) * W/nf * 0.29'
+ as='int((nf+2)/2) * W/nf * 0.29' pd='2*int((nf+1)/2) * (W/nf + 0.29)' ps='2*int((nf+2)/2) * (W/nf + 0.29)'
+ nrd='0.29 / W' nrs='0.29 / W' sa=0 sb=0 sd=0 mult=1 m=1
XM68 net29 net30 VDDA VDDA sky130_fd_pr__pfet_01v8 L=0.15 W=0.5 nf=1 ad='int((nf+1)/2) * W/nf * 0.29'
+ as='int((nf+2)/2) * W/nf * 0.29' pd='2*int((nf+1)/2) * (W/nf + 0.29)' ps='2*int((nf+2)/2) * (W/nf + 0.29)'
+ nrd='0.29 / W' nrs='0.29 / W' sa=0 sb=0 sd=0 mult=1 m=1
XM69 net29 CLK3 GNDA GNDA sky130_fd_pr__nfet_01v8 L=0.15 W=1.5 nf=1 ad='int((nf+1)/2) * W/nf * 0.29'
+ as='int((nf+2)/2) * W/nf * 0.29' pd='2*int((nf+1)/2) * (W/nf + 0.29)' ps='2*int((nf+2)/2) * (W/nf + 0.29)'
+ nrd='0.29 / W' nrs='0.29 / W' sa=0 sb=0 sd=0 mult=1 m=1
XM70 net30 VIN4 VDDA VDDA sky130_fd_pr__pfet_01v8 L=0.15 W=0.5 nf=1 ad='int((nf+1)/2) * W/nf * 0.29'
+ as='int((nf+2)/2) * W/nf * 0.29' pd='2*int((nf+1)/2) * (W/nf + 0.29)' ps='2*int((nf+2)/2) * (W/nf + 0.29)'
+ nrd='0.29 / W' nrs='0.29 / W' sa=0 sb=0 sd=0 mult=1 m=1
XM71 net31 VIN4 GNDA GNDA sky130_fd_pr__nfet_01v8 L=0.15 W=0.5 nf=1 ad='int((nf+1)/2) * W/nf * 0.29'
+ as='int((nf+2)/2) * W/nf * 0.29' pd='2*int((nf+1)/2) * (W/nf + 0.29)' ps='2*int((nf+2)/2) * (W/nf + 0.29)'
+ nrd='0.29 / W' nrs='0.29 / W' sa=0 sb=0 sd=0 mult=1 m=1
XM72 net30 CLK3 net31 GNDA sky130_fd_pr__nfet_01v8 L=0.15 W=0.5 nf=1 ad='int((nf+1)/2) * W/nf * 0.29'
+ as='int((nf+2)/2) * W/nf * 0.29' pd='2*int((nf+1)/2) * (W/nf + 0.29)' ps='2*int((nf+2)/2) * (W/nf + 0.29)'
+ nrd='0.29 / W' nrs='0.29 / W' sa=0 sb=0 sd=0 mult=1 m=1
XM73 CLK3 VIN3 VDDA VDDA sky130_fd_pr__pfet_01v8 L=0.15 W=1.0 nf=2 ad='int((nf+1)/2) * W/nf * 0.29' as='int((nf+2)/2) * W/nf * 0.29'
+ pd='2*int((nf+1)/2) * (W/nf + 0.29)' ps='2*int((nf+2)/2) * (W/nf + 0.29)' nrd='0.29 / W' nrs='0.29 / W'
+ sa=0 sb=0 sd=0 mult=1 m=1
XM74 CLK3 VIN3 GNDA GNDA sky130_fd_pr__nfet_01v8 L=0.15 W=0.5 nf=1 ad='int((nf+1)/2) * W/nf * 0.29' as='int((nf+2)/2) * W/nf * 0.29'
+ pd='2*int((nf+1)/2) * (W/nf + 0.29)' ps='2*int((nf+2)/2) * (W/nf + 0.29)' nrd='0.29 / W' nrs='0.29 / W'
+ sa=0 sb=0 sd=0 mult=1 m=1
**.ends
.end
